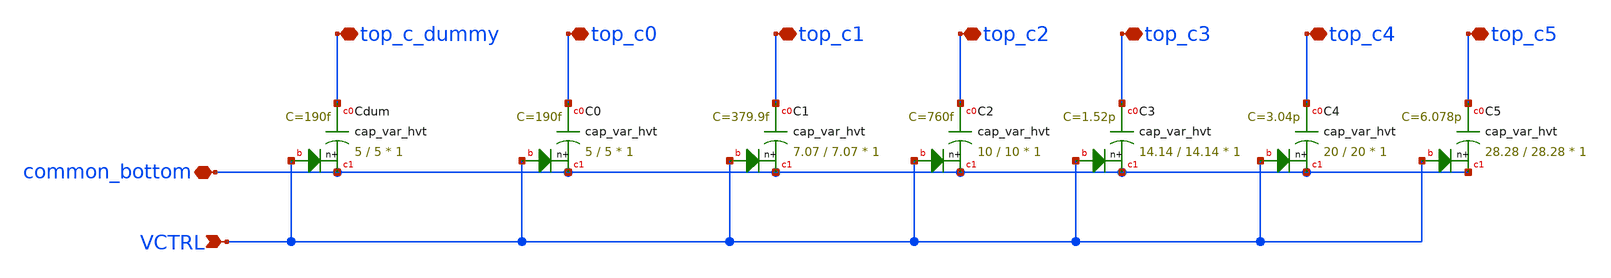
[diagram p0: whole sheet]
** sch_path: SKY130/SAR-ADC/SAR-ADC_5.0V/cap_array_var_1unit.sch
**.subckt cap_array_var_1unit common_bottom top_c1 top_c0 top_c_dummy top_c2 top_c4 top_c5 top_c3
*+ VCTRL
*.iopin common_bottom
*.iopin top_c1
*.iopin top_c0
*.iopin top_c_dummy
*.iopin top_c2
*.iopin top_c4
*.iopin top_c5
*.iopin top_c3
*.ipin VCTRL
XC0 top_c0 common_bottom VCTRL sky130_fd_pr__cap_var_hvt W=5 L=5 VM=1 m=1
XC1 top_c1 common_bottom VCTRL sky130_fd_pr__cap_var_hvt W=7.07 L=7.07 VM=1 m=1
XC2 top_c2 common_bottom VCTRL sky130_fd_pr__cap_var_hvt W=10 L=10 VM=1 m=1
XC3 top_c3 common_bottom VCTRL sky130_fd_pr__cap_var_hvt W=14.14 L=14.14 VM=1 m=1
XC4 top_c4 common_bottom VCTRL sky130_fd_pr__cap_var_hvt W=20 L=20 VM=1 m=1
XC5 top_c5 common_bottom VCTRL sky130_fd_pr__cap_var_hvt W=28.28 L=28.28 VM=1 m=1
XCdum top_c_dummy common_bottom VCTRL sky130_fd_pr__cap_var_hvt W=5 L=5 VM=1 m=1
**.ends
.end
